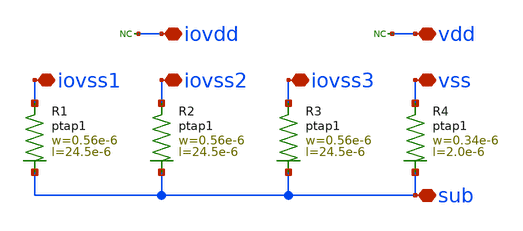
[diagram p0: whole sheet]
** sch_path: MSPHY6034-main/schematic/xschem/openpdk-libraries/ihp-sg13g2/sg13g2_io/xschem/sg13g2_Filler200.sch
**.subckt sg13g2_Filler200 iovss1 iovss2 iovss3 vss iovdd vdd sub
*.iopin iovss1
*.iopin iovss2
*.iopin iovss3
*.iopin vss
*.iopin iovdd
*.iopin vdd
*.iopin sub
XR3 iovss3 sub ptap1 R=15.35 w=0.56e-6 l=24.5e-6
XR4 vss sub ptap1 R=182.8 w=0.34e-6 l=2.0e-6
XR1 iovss1 sub ptap1 R=15.35 w=0.56e-6 l=24.5e-6
XR2 iovss2 sub ptap1 R=15.35 w=0.56e-6 l=24.5e-6
* noconn iovdd
* noconn vdd
**.ends
.end
